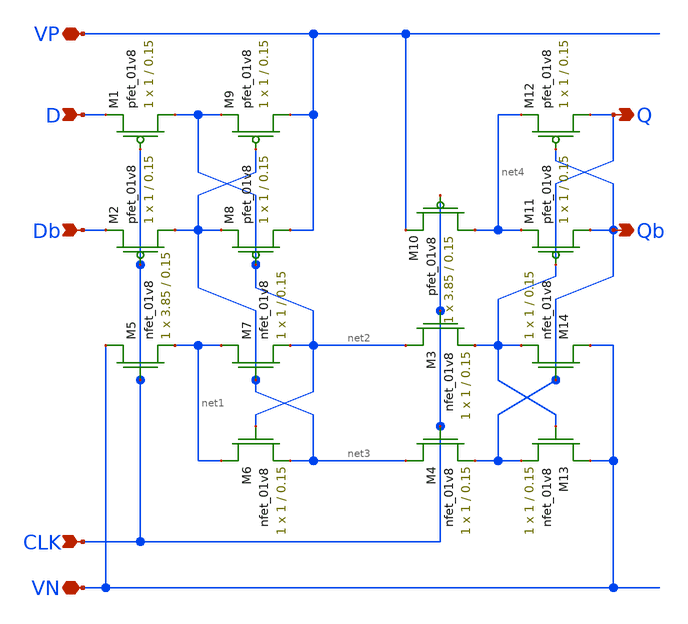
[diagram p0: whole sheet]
** sch_path: mp2/flipflop_layout.sch
**.subckt flipflop_layout D Db CLK Q Qb VP VN
*.ipin D
*.ipin Db
*.ipin CLK
*.opin Q
*.opin Qb
*.iopin VP
*.iopin VN
XM1 net2 CLK D VDD sky130_fd_pr__pfet_01v8 L=0.15 W=1 nf=1 ad='int((nf+1)/2) * W/nf * 0.29' as='int((nf+2)/2) * W/nf * 0.29'
+ pd='2*int((nf+1)/2) * (W/nf + 0.29)' ps='2*int((nf+2)/2) * (W/nf + 0.29)' nrd='0.29 / W' nrs='0.29 / W'
+ sa=0 sb=0 sd=0 mult=1 m=1
XM2 net3 CLK Db VDD sky130_fd_pr__pfet_01v8 L=0.15 W=1 nf=1 ad='int((nf+1)/2) * W/nf * 0.29' as='int((nf+2)/2) * W/nf * 0.29'
+ pd='2*int((nf+1)/2) * (W/nf + 0.29)' ps='2*int((nf+2)/2) * (W/nf + 0.29)' nrd='0.29 / W' nrs='0.29 / W'
+ sa=0 sb=0 sd=0 mult=1 m=1
XM3 net2 CLK Q GND sky130_fd_pr__nfet_01v8 L=0.15 W=1 nf=1 ad='int((nf+1)/2) * W/nf * 0.29' as='int((nf+2)/2) * W/nf * 0.29'
+ pd='2*int((nf+1)/2) * (W/nf + 0.29)' ps='2*int((nf+2)/2) * (W/nf + 0.29)' nrd='0.29 / W' nrs='0.29 / W'
+ sa=0 sb=0 sd=0 mult=1 m=1
XM4 net3 CLK Qb GND sky130_fd_pr__nfet_01v8 L=0.15 W=1 nf=1 ad='int((nf+1)/2) * W/nf * 0.29' as='int((nf+2)/2) * W/nf * 0.29'
+ pd='2*int((nf+1)/2) * (W/nf + 0.29)' ps='2*int((nf+2)/2) * (W/nf + 0.29)' nrd='0.29 / W' nrs='0.29 / W'
+ sa=0 sb=0 sd=0 mult=1 m=1
XM5 VN CLK net1 GND sky130_fd_pr__nfet_01v8 L=0.15 W=3.85 nf=1 ad='int((nf+1)/2) * W/nf * 0.29' as='int((nf+2)/2) * W/nf * 0.29'
+ pd='2*int((nf+1)/2) * (W/nf + 0.29)' ps='2*int((nf+2)/2) * (W/nf + 0.29)' nrd='0.29 / W' nrs='0.29 / W'
+ sa=0 sb=0 sd=0 mult=1 m=1
XM6 net1 net2 net3 GND sky130_fd_pr__nfet_01v8 L=0.15 W=1 nf=1 ad='int((nf+1)/2) * W/nf * 0.29' as='int((nf+2)/2) * W/nf * 0.29'
+ pd='2*int((nf+1)/2) * (W/nf + 0.29)' ps='2*int((nf+2)/2) * (W/nf + 0.29)' nrd='0.29 / W' nrs='0.29 / W'
+ sa=0 sb=0 sd=0 mult=1 m=1
XM7 net1 net3 net2 GND sky130_fd_pr__nfet_01v8 L=0.15 W=1 nf=1 ad='int((nf+1)/2) * W/nf * 0.29' as='int((nf+2)/2) * W/nf * 0.29'
+ pd='2*int((nf+1)/2) * (W/nf + 0.29)' ps='2*int((nf+2)/2) * (W/nf + 0.29)' nrd='0.29 / W' nrs='0.29 / W'
+ sa=0 sb=0 sd=0 mult=1 m=1
XM8 VP net2 net3 VDD sky130_fd_pr__pfet_01v8 L=0.15 W=1 nf=1 ad='int((nf+1)/2) * W/nf * 0.29' as='int((nf+2)/2) * W/nf * 0.29'
+ pd='2*int((nf+1)/2) * (W/nf + 0.29)' ps='2*int((nf+2)/2) * (W/nf + 0.29)' nrd='0.29 / W' nrs='0.29 / W'
+ sa=0 sb=0 sd=0 mult=1 m=1
XM9 VP net3 net2 VDD sky130_fd_pr__pfet_01v8 L=0.15 W=1 nf=1 ad='int((nf+1)/2) * W/nf * 0.29' as='int((nf+2)/2) * W/nf * 0.29'
+ pd='2*int((nf+1)/2) * (W/nf + 0.29)' ps='2*int((nf+2)/2) * (W/nf + 0.29)' nrd='0.29 / W' nrs='0.29 / W'
+ sa=0 sb=0 sd=0 mult=1 m=1
XM10 net4 CLK VP VDD sky130_fd_pr__pfet_01v8 L=0.15 W=3.85 nf=1 ad='int((nf+1)/2) * W/nf * 0.29' as='int((nf+2)/2) * W/nf * 0.29'
+ pd='2*int((nf+1)/2) * (W/nf + 0.29)' ps='2*int((nf+2)/2) * (W/nf + 0.29)' nrd='0.29 / W' nrs='0.29 / W'
+ sa=0 sb=0 sd=0 mult=1 m=1
XM11 Qb Q net4 VDD sky130_fd_pr__pfet_01v8 L=0.15 W=1 nf=1 ad='int((nf+1)/2) * W/nf * 0.29' as='int((nf+2)/2) * W/nf * 0.29'
+ pd='2*int((nf+1)/2) * (W/nf + 0.29)' ps='2*int((nf+2)/2) * (W/nf + 0.29)' nrd='0.29 / W' nrs='0.29 / W'
+ sa=0 sb=0 sd=0 mult=1 m=1
XM12 Q Qb net4 VDD sky130_fd_pr__pfet_01v8 L=0.15 W=1 nf=1 ad='int((nf+1)/2) * W/nf * 0.29' as='int((nf+2)/2) * W/nf * 0.29'
+ pd='2*int((nf+1)/2) * (W/nf + 0.29)' ps='2*int((nf+2)/2) * (W/nf + 0.29)' nrd='0.29 / W' nrs='0.29 / W'
+ sa=0 sb=0 sd=0 mult=1 m=1
XM13 VN Q Qb GND sky130_fd_pr__nfet_01v8 L=0.15 W=1 nf=1 ad='int((nf+1)/2) * W/nf * 0.29' as='int((nf+2)/2) * W/nf * 0.29'
+ pd='2*int((nf+1)/2) * (W/nf + 0.29)' ps='2*int((nf+2)/2) * (W/nf + 0.29)' nrd='0.29 / W' nrs='0.29 / W'
+ sa=0 sb=0 sd=0 mult=1 m=1
XM14 VN Qb Q GND sky130_fd_pr__nfet_01v8 L=0.15 W=1 nf=1 ad='int((nf+1)/2) * W/nf * 0.29' as='int((nf+2)/2) * W/nf * 0.29'
+ pd='2*int((nf+1)/2) * (W/nf + 0.29)' ps='2*int((nf+2)/2) * (W/nf + 0.29)' nrd='0.29 / W' nrs='0.29 / W'
+ sa=0 sb=0 sd=0 mult=1 m=1
**.ends
.end
